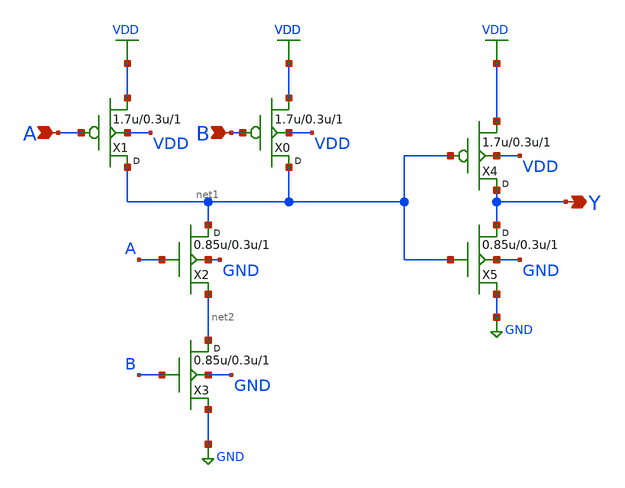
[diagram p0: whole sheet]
** sch_path: openfasoc/common/platforms/gf180osu9t/lib/and21/gf180mcu_osu_sc_and2_1.sch
**.subckt gf180mcu_osu_sc_and2_1 A B Y
*.ipin A
*.ipin B
*.opin Y
X1 net1 A VDD VDD pmos_3p3 w=1.7u l=0.3u m=1
X0 net1 B VDD VDD pmos_3p3 w=1.7u l=0.3u m=1
X2 net1 A net2 GND nmos_3p3 w=0.85u l=0.3u m=1
X3 net2 B GND GND nmos_3p3 w=0.85u l=0.3u m=1
X4 Y net1 VDD VDD pmos_3p3 w=1.7u l=0.3u m=1
X5 Y net1 GND GND nmos_3p3 w=0.85u l=0.3u m=1
**.ends
.GLOBAL VDD
.GLOBAL GND
.end
